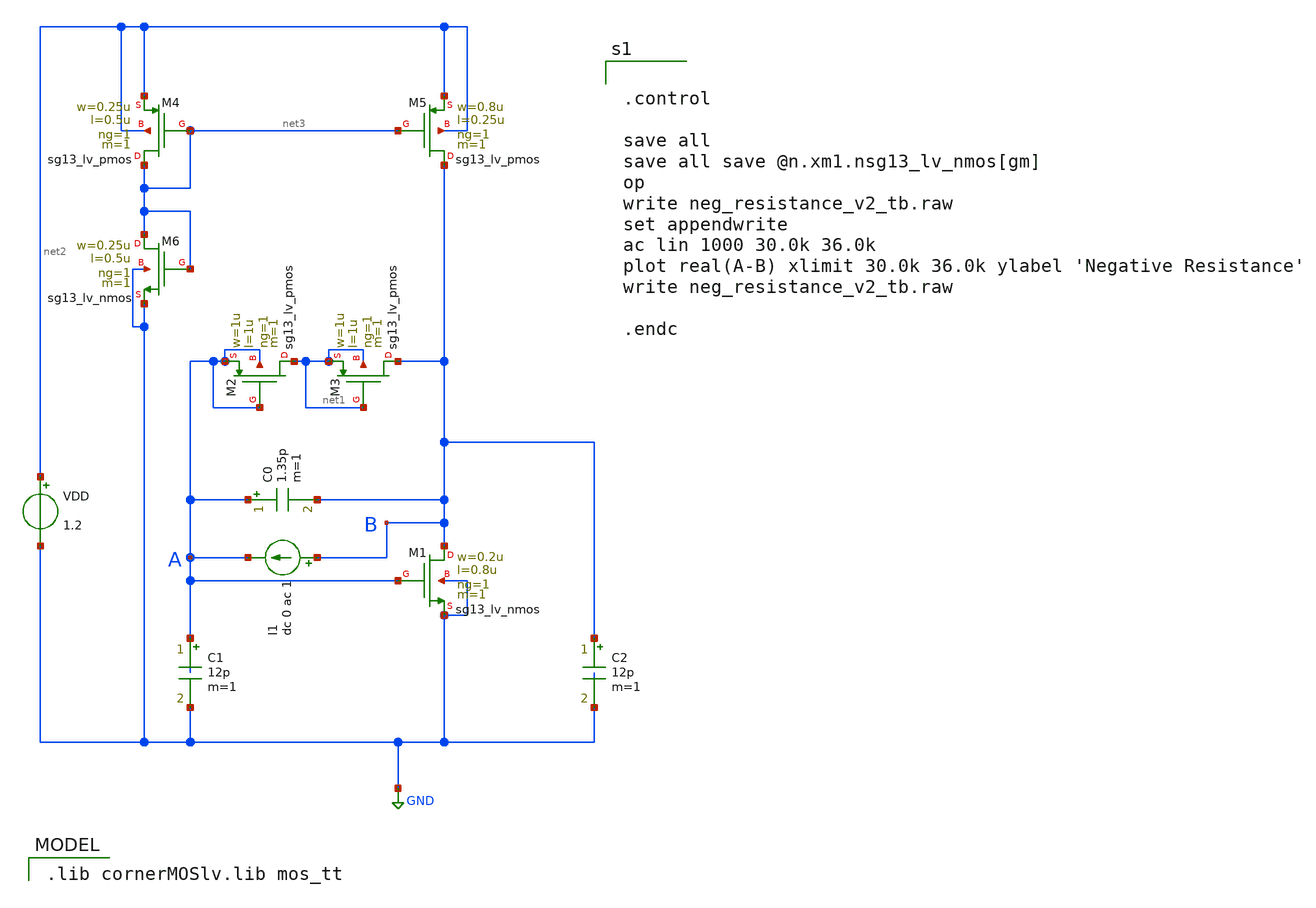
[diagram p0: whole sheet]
** sch_path: neg_resistance_v2_tb.sch
**.subckt neg_resistance_v2_tb
XM1 B A GND GND sg13_lv_nmos w=0.2u l=0.8u ng=1 m=1 mm_ok=1
C1 A GND 12p m=1
C2 B GND 12p m=1
C0 A B 1.35p m=1
VDD net2 GND 1.2
I1 B A dc 0 ac 1
XM2 net1 A A A sg13_lv_pmos w=1u l=1u ng=1 m=1 mm_ok=1
XM3 B net1 net1 net1 sg13_lv_pmos w=1u l=1u ng=1 m=1 mm_ok=1
XM4 net3 net3 net2 net2 sg13_lv_pmos w=0.25u l=0.5u ng=1 m=1 mm_ok=1
XM5 B net3 net2 net2 sg13_lv_pmos w=0.8u l=0.25u ng=1 m=1 mm_ok=1
XM6 net3 net3 GND GND sg13_lv_nmos w=0.25u l=0.5u ng=1 m=1 mm_ok=1
**** begin user architecture code


.control

save all
save all save @n.xm1.nsg13_lv_nmos[gm]
op
write neg_resistance_v2_tb.raw
set appendwrite
ac lin 1000 30.0k 36.0k
plot real(A-B) xlimit 30.0k 36.0k ylabel 'Negative Resistance'
write neg_resistance_v2_tb.raw

.endc


 .lib cornerMOSlv.lib mos_tt

**** end user architecture code
**.ends
.GLOBAL GND
.end
